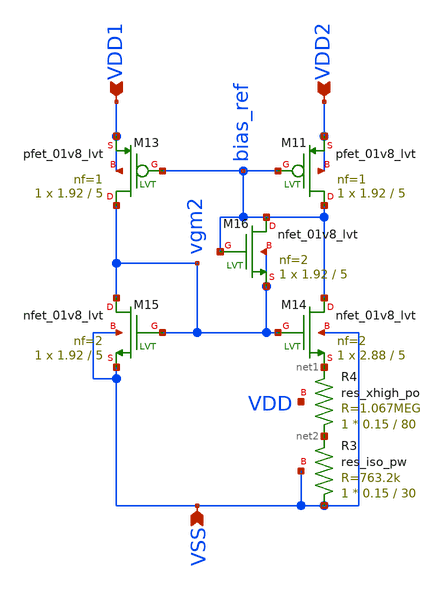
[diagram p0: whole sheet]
** sch_path: design/LELO_SVOD_SKY130A/LELO_PTAT_CURRENT.sch
**.subckt LELO_PTAT_CURRENT VDD1 VSS VDD2
*.ipin VDD1
*.ipin VSS
*.ipin VDD2
XM11 bias_ref bias_ref VDD2 VDD2 sky130_fd_pr__pfet_01v8_lvt L=5 W=1.92 nf=1 ad='int((1 + 1)/2) * 1.92 / 1 * 0.29'
+ as='int((1 + 2)/2) * 1.92 / 1 * 0.29' pd='2*int((1 + 1)/2) * (1.92 / 1 + 0.29)' ps='2*int((1 + 2)/2) * (1.92 / 1 + 0.29)'
+ nrd='0.29 / 1.92 ' nrs='0.29 / 1.92 ' sa=0 sb=0 sd=0 mult=1 m=1
XM13 vgm2 bias_ref VDD1 VDD1 sky130_fd_pr__pfet_01v8_lvt L=5 W=1.92 nf=1 ad='int((1 + 1)/2) * 1.92 / 1 * 0.29'
+ as='int((1 + 2)/2) * 1.92 / 1 * 0.29' pd='2*int((1 + 1)/2) * (1.92 / 1 + 0.29)' ps='2*int((1 + 2)/2) * (1.92 / 1 + 0.29)'
+ nrd='0.29 / 1.92 ' nrs='0.29 / 1.92 ' sa=0 sb=0 sd=0 mult=1 m=1
XM14 bias_ref vgm2 net1 VSS sky130_fd_pr__nfet_01v8_lvt L=5 W=2.88 nf=2 ad='int((2 + 1)/2) * 2.88 / 2 * 0.29'
+ as='int((2 + 2)/2) * 2.88 / 2 * 0.29' pd='2*int((2 + 1)/2) * (2.88 / 2 + 0.29)' ps='2*int((2 + 2)/2) * (2.88 / 2 + 0.29)'
+ nrd='0.29 / 2.88 ' nrs='0.29 / 2.88 ' sa=0 sb=0 sd=0 mult=1 m=1
XM15 vgm2 vgm2 VSS VSS sky130_fd_pr__nfet_01v8_lvt L=5 W=1.92 nf=2 ad='int((2 + 1)/2) * 1.92 / 2 * 0.29'
+ as='int((2 + 2)/2) * 1.92 / 2 * 0.29' pd='2*int((2 + 1)/2) * (1.92 / 2 + 0.29)' ps='2*int((2 + 2)/2) * (1.92 / 2 + 0.29)'
+ nrd='0.29 / 1.92 ' nrs='0.29 / 1.92 ' sa=0 sb=0 sd=0 mult=1 m=1
XM16 bias_ref bias_ref vgm2 vgm2 sky130_fd_pr__nfet_01v8_lvt L=5 W=1.92 nf=2 ad='int((2 + 1)/2) * 1.92 / 2 * 0.29'
+ as='int((2 + 2)/2) * 1.92 / 2 * 0.29' pd='2*int((2 + 1)/2) * (1.92 / 2 + 0.29)' ps='2*int((2 + 2)/2) * (1.92 / 2 + 0.29)'
+ nrd='0.29 / 1.92 ' nrs='0.29 / 1.92 ' sa=0 sb=0 sd=0 mult=1 m=1
XR3 VSS net2 VSS sky130_fd_pr__res_iso_pw W=0.15 L=30 m=1
XR4 net2 net1 VDD sky130_fd_pr__res_xhigh_po W=0.15 L=80 mult=1 m=1
**.ends
.end
